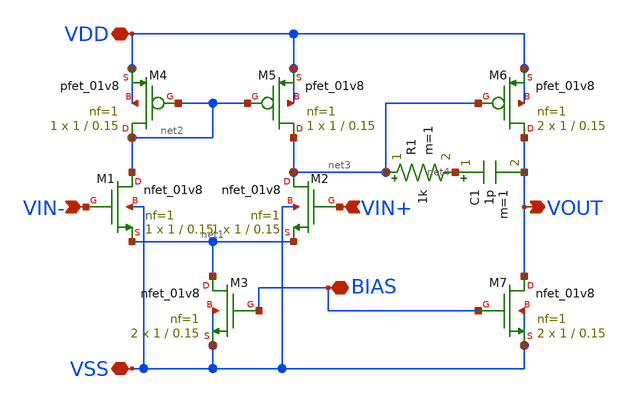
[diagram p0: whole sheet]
** sch_path: analog/bootcamp_opamp/schematics/opamp_two_stage.sch
**.subckt opamp_two_stage VIN- VSS VIN+ VOUT VDD BIAS
*.ipin VIN-
*.iopin VSS
*.ipin VIN+
*.opin VOUT
*.iopin VDD
*.iopin BIAS
XM1 net2 VIN- net1 VSS sky130_fd_pr__nfet_01v8 L=0.15 W=1 nf=1 ad='int((nf+1)/2) * W/nf * 0.29' as='int((nf+2)/2) * W/nf * 0.29'
+ pd='2*int((nf+1)/2) * (W/nf + 0.29)' ps='2*int((nf+2)/2) * (W/nf + 0.29)' nrd='0.29 / W' nrs='0.29 / W'
+ sa=0 sb=0 sd=0 mult=1 m=1
XM2 net3 VIN+ net1 VSS sky130_fd_pr__nfet_01v8 L=0.15 W=1 nf=1 ad='int((nf+1)/2) * W/nf * 0.29' as='int((nf+2)/2) * W/nf * 0.29'
+ pd='2*int((nf+1)/2) * (W/nf + 0.29)' ps='2*int((nf+2)/2) * (W/nf + 0.29)' nrd='0.29 / W' nrs='0.29 / W'
+ sa=0 sb=0 sd=0 mult=1 m=1
XM3 net1 BIAS VSS VSS sky130_fd_pr__nfet_01v8 L=0.15 W=1 nf=1 ad='int((nf+1)/2) * W/nf * 0.29' as='int((nf+2)/2) * W/nf * 0.29'
+ pd='2*int((nf+1)/2) * (W/nf + 0.29)' ps='2*int((nf+2)/2) * (W/nf + 0.29)' nrd='0.29 / W' nrs='0.29 / W'
+ sa=0 sb=0 sd=0 mult=2 m=2
XM7 VOUT BIAS VSS VSS sky130_fd_pr__nfet_01v8 L=0.15 W=1 nf=1 ad='int((nf+1)/2) * W/nf * 0.29' as='int((nf+2)/2) * W/nf * 0.29'
+ pd='2*int((nf+1)/2) * (W/nf + 0.29)' ps='2*int((nf+2)/2) * (W/nf + 0.29)' nrd='0.29 / W' nrs='0.29 / W'
+ sa=0 sb=0 sd=0 mult=2 m=2
XM4 net2 net2 VDD VDD sky130_fd_pr__pfet_01v8 L=0.15 W=1 nf=1 ad='int((nf+1)/2) * W/nf * 0.29' as='int((nf+2)/2) * W/nf * 0.29'
+ pd='2*int((nf+1)/2) * (W/nf + 0.29)' ps='2*int((nf+2)/2) * (W/nf + 0.29)' nrd='0.29 / W' nrs='0.29 / W'
+ sa=0 sb=0 sd=0 mult=1 m=1
XM5 net3 net2 VDD VDD sky130_fd_pr__pfet_01v8 L=0.15 W=1 nf=1 ad='int((nf+1)/2) * W/nf * 0.29' as='int((nf+2)/2) * W/nf * 0.29'
+ pd='2*int((nf+1)/2) * (W/nf + 0.29)' ps='2*int((nf+2)/2) * (W/nf + 0.29)' nrd='0.29 / W' nrs='0.29 / W'
+ sa=0 sb=0 sd=0 mult=1 m=1
XM6 VOUT net3 VDD VDD sky130_fd_pr__pfet_01v8 L=0.15 W=1 nf=1 ad='int((nf+1)/2) * W/nf * 0.29' as='int((nf+2)/2) * W/nf * 0.29'
+ pd='2*int((nf+1)/2) * (W/nf + 0.29)' ps='2*int((nf+2)/2) * (W/nf + 0.29)' nrd='0.29 / W' nrs='0.29 / W'
+ sa=0 sb=0 sd=0 mult=2 m=2
R1 net3 net4 1k m=1
C1 net4 VOUT 1p m=1
**.ends
.end
